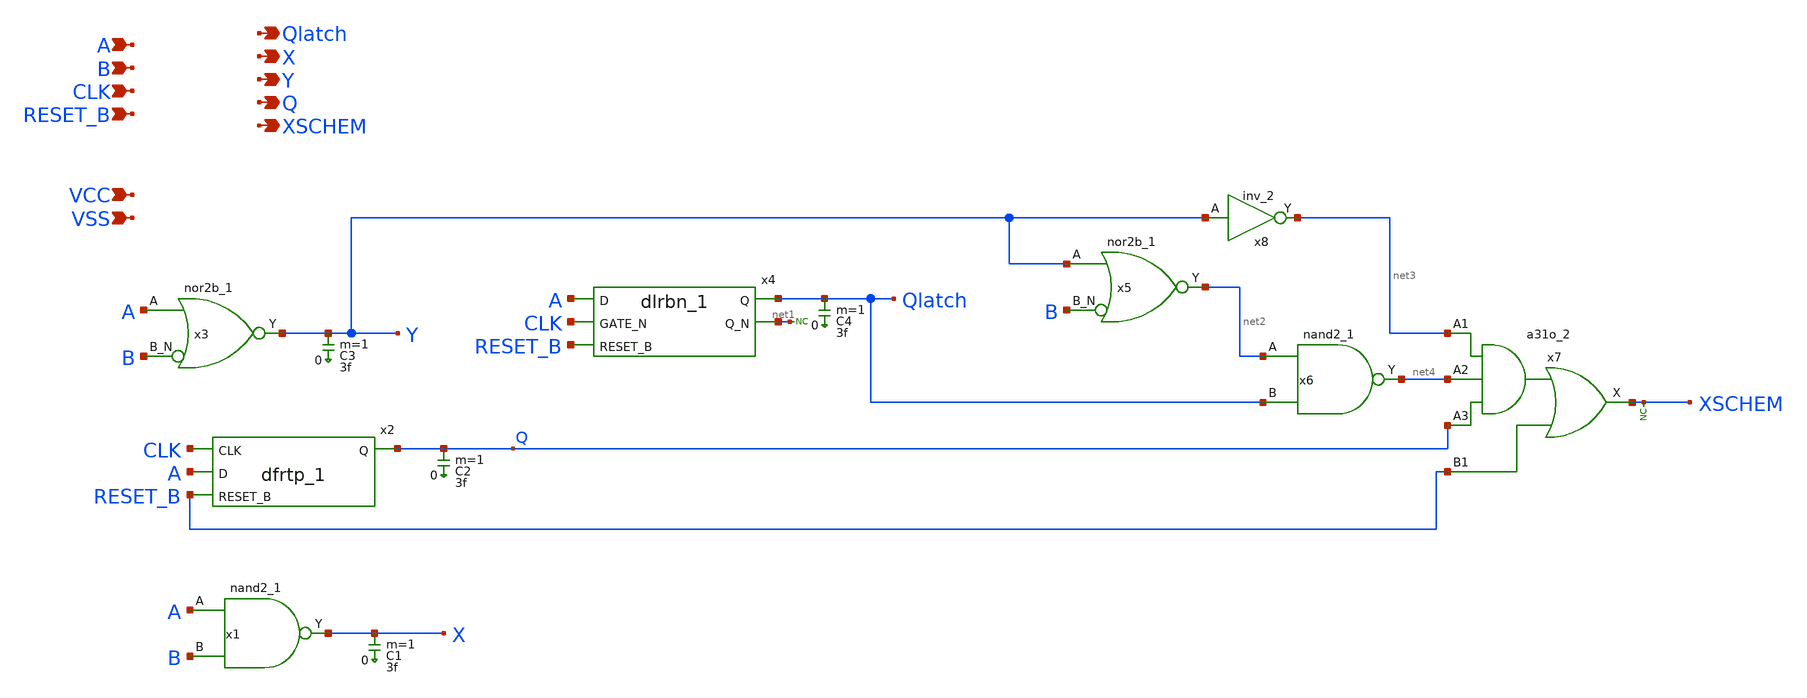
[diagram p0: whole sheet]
** sch_path: sky130_tests/stdcells.sch
* Copyright 2021 Stefan Frederik Schippers
* Licensed under the Apache License, Version 2.0 (the "License");
* you may not use this file except in compliance with the License.
* You may obtain a copy of the License at
* https://www.apache.org/licenses/LICENSE-2.0
* Unless required by applicable law or agreed to in writing, software
* distributed under the License is distributed on an "AS IS" BASIS,
* WITHOUT WARRANTIES OR CONDITIONS OF ANY KIND, either express or implied.
* See the License for the specific language governing permissions and
* limitations under the License.
**.subckt stdcells RESET_B CLK B A Y X Qlatch Q XSCHEM VCC VSS
*.ipin RESET_B
*.ipin CLK
*.ipin B
*.ipin A
*.opin Y
*.opin X
*.opin Qlatch
*.opin Q
*.opin XSCHEM
*.ipin VCC
*.ipin VSS
x1 A B VSS VSS VCC VCC X sky130_fd_sc_hd__nand2_1
C1 X 0 3f m=1
x2 CLK A RESET_B VSS VSS VCC VCC Q sky130_fd_sc_hd__dfrtp_1
C2 Q 0 3f m=1
C3 Y 0 3f m=1
x3 A B VSS VSS VCC VCC Y sky130_fd_sc_hd__nor2b_1
x4 A CLK RESET_B VSS VSS VCC VCC Qlatch net1 sky130_fd_sc_hd__dlrbn_1
C4 Qlatch 0 3f m=1
x5 Y B VSS VSS VCC VCC net2 sky130_fd_sc_hd__nor2b_1
x6 net2 Qlatch VSS VSS VCC VCC net4 sky130_fd_sc_hd__nand2_1
x7 net3 net4 Q RESET_B VSS VSS VCC VCC XSCHEM sky130_fd_sc_hd__a31o_2
* noconn #net1
* noconn XSCHEM
x8 Y VSS VSS VCC VCC net3 sky130_fd_sc_hd__inv_2
**.ends
.end
